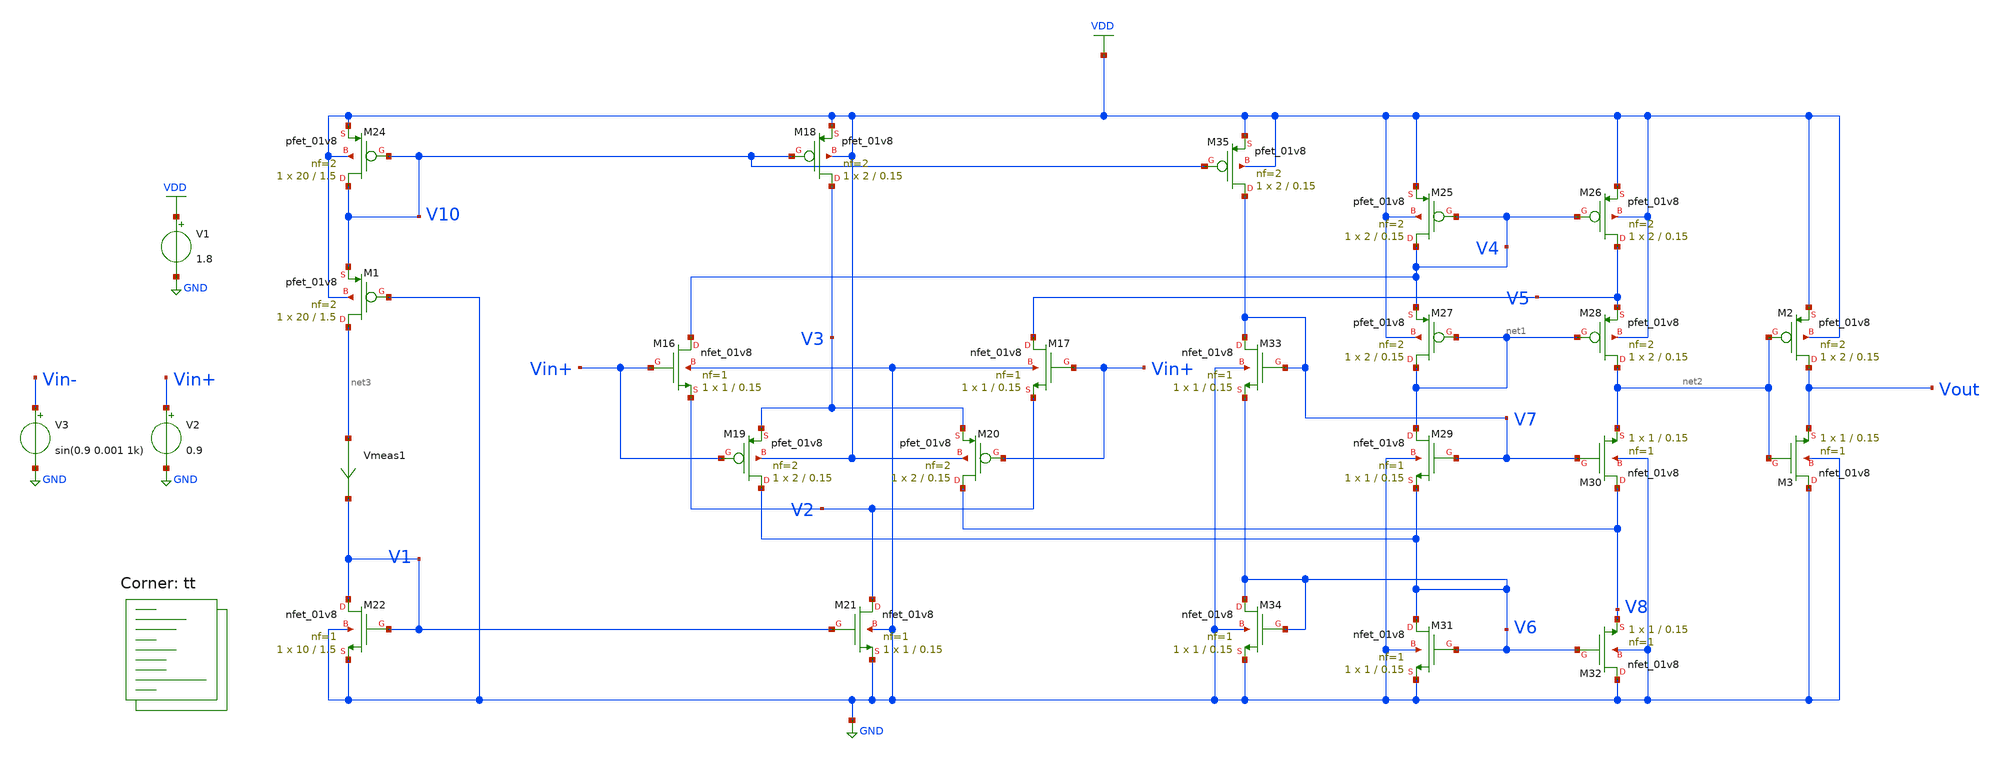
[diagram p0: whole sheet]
** sch_path: projects/pll/charge_pump/xschem_ngspice/tb_rail_to_rail_opamp2.sch
**.subckt tb_rail_to_rail_opamp2
V1 VDD GND 1.8
V3 Vin- GND sin(0.9 0.001 1k)
V2 Vin+ GND 0.9
XM16 V4 Vin+ V2 GND sky130_fd_pr__nfet_01v8 L=0.15 W=1 nf=1 ad='int((nf+1)/2) * W/nf * 0.29' as='int((nf+2)/2) * W/nf * 0.29'
+ pd='2*int((nf+1)/2) * (W/nf + 0.29)' ps='2*int((nf+2)/2) * (W/nf + 0.29)' nrd='0.29 / W' nrs='0.29 / W'
+ sa=0 sb=0 sd=0 mult=1 m=1
XM17 V5 Vin+ V2 GND sky130_fd_pr__nfet_01v8 L=0.15 W=1 nf=1 ad='int((nf+1)/2) * W/nf * 0.29' as='int((nf+2)/2) * W/nf * 0.29'
+ pd='2*int((nf+1)/2) * (W/nf + 0.29)' ps='2*int((nf+2)/2) * (W/nf + 0.29)' nrd='0.29 / W' nrs='0.29 / W'
+ sa=0 sb=0 sd=0 mult=1 m=1
XM18 V3 V10 VDD VDD sky130_fd_pr__pfet_01v8 L=0.15 W=2 nf=2 ad='int((nf+1)/2) * W/nf * 0.29' as='int((nf+2)/2) * W/nf * 0.29'
+ pd='2*int((nf+1)/2) * (W/nf + 0.29)' ps='2*int((nf+2)/2) * (W/nf + 0.29)' nrd='0.29 / W' nrs='0.29 / W'
+ sa=0 sb=0 sd=0 mult=1 m=1
XM19 V6 Vin+ V3 VDD sky130_fd_pr__pfet_01v8 L=0.15 W=2 nf=2 ad='int((nf+1)/2) * W/nf * 0.29' as='int((nf+2)/2) * W/nf * 0.29'
+ pd='2*int((nf+1)/2) * (W/nf + 0.29)' ps='2*int((nf+2)/2) * (W/nf + 0.29)' nrd='0.29 / W' nrs='0.29 / W'
+ sa=0 sb=0 sd=0 mult=1 m=1
XM20 V8 Vin+ V3 VDD sky130_fd_pr__pfet_01v8 L=0.15 W=2 nf=2 ad='int((nf+1)/2) * W/nf * 0.29' as='int((nf+2)/2) * W/nf * 0.29'
+ pd='2*int((nf+1)/2) * (W/nf + 0.29)' ps='2*int((nf+2)/2) * (W/nf + 0.29)' nrd='0.29 / W' nrs='0.29 / W'
+ sa=0 sb=0 sd=0 mult=1 m=1
XM21 V2 V1 GND GND sky130_fd_pr__nfet_01v8 L=0.15 W=1 nf=1 ad='int((nf+1)/2) * W/nf * 0.29' as='int((nf+2)/2) * W/nf * 0.29'
+ pd='2*int((nf+1)/2) * (W/nf + 0.29)' ps='2*int((nf+2)/2) * (W/nf + 0.29)' nrd='0.29 / W' nrs='0.29 / W'
+ sa=0 sb=0 sd=0 mult=1 m=1
XM22 V1 V1 GND GND sky130_fd_pr__nfet_01v8 L=1.5 W=10 nf=1 ad='int((nf+1)/2) * W/nf * 0.29' as='int((nf+2)/2) * W/nf * 0.29'
+ pd='2*int((nf+1)/2) * (W/nf + 0.29)' ps='2*int((nf+2)/2) * (W/nf + 0.29)' nrd='0.29 / W' nrs='0.29 / W'
+ sa=0 sb=0 sd=0 mult=1 m=1
XM24 V10 V10 VDD VDD sky130_fd_pr__pfet_01v8 L=1.5 W=20 nf=2 ad='int((nf+1)/2) * W/nf * 0.29' as='int((nf+2)/2) * W/nf * 0.29'
+ pd='2*int((nf+1)/2) * (W/nf + 0.29)' ps='2*int((nf+2)/2) * (W/nf + 0.29)' nrd='0.29 / W' nrs='0.29 / W'
+ sa=0 sb=0 sd=0 mult=1 m=1
XM25 V4 V4 VDD VDD sky130_fd_pr__pfet_01v8 L=0.15 W=2 nf=2 ad='int((nf+1)/2) * W/nf * 0.29' as='int((nf+2)/2) * W/nf * 0.29'
+ pd='2*int((nf+1)/2) * (W/nf + 0.29)' ps='2*int((nf+2)/2) * (W/nf + 0.29)' nrd='0.29 / W' nrs='0.29 / W'
+ sa=0 sb=0 sd=0 mult=1 m=1
XM26 V5 V4 VDD VDD sky130_fd_pr__pfet_01v8 L=0.15 W=2 nf=2 ad='int((nf+1)/2) * W/nf * 0.29' as='int((nf+2)/2) * W/nf * 0.29'
+ pd='2*int((nf+1)/2) * (W/nf + 0.29)' ps='2*int((nf+2)/2) * (W/nf + 0.29)' nrd='0.29 / W' nrs='0.29 / W'
+ sa=0 sb=0 sd=0 mult=1 m=1
XM27 net1 net1 V4 VDD sky130_fd_pr__pfet_01v8 L=0.15 W=2 nf=2 ad='int((nf+1)/2) * W/nf * 0.29' as='int((nf+2)/2) * W/nf * 0.29'
+ pd='2*int((nf+1)/2) * (W/nf + 0.29)' ps='2*int((nf+2)/2) * (W/nf + 0.29)' nrd='0.29 / W' nrs='0.29 / W'
+ sa=0 sb=0 sd=0 mult=1 m=1
XM28 net2 net1 V5 VDD sky130_fd_pr__pfet_01v8 L=0.15 W=2 nf=2 ad='int((nf+1)/2) * W/nf * 0.29' as='int((nf+2)/2) * W/nf * 0.29'
+ pd='2*int((nf+1)/2) * (W/nf + 0.29)' ps='2*int((nf+2)/2) * (W/nf + 0.29)' nrd='0.29 / W' nrs='0.29 / W'
+ sa=0 sb=0 sd=0 mult=1 m=1
XM29 net1 V7 V6 GND sky130_fd_pr__nfet_01v8 L=0.15 W=1 nf=1 ad='int((nf+1)/2) * W/nf * 0.29' as='int((nf+2)/2) * W/nf * 0.29'
+ pd='2*int((nf+1)/2) * (W/nf + 0.29)' ps='2*int((nf+2)/2) * (W/nf + 0.29)' nrd='0.29 / W' nrs='0.29 / W'
+ sa=0 sb=0 sd=0 mult=1 m=1
XM30 V8 V7 net2 GND sky130_fd_pr__nfet_01v8 L=0.15 W=1 nf=1 ad='int((nf+1)/2) * W/nf * 0.29' as='int((nf+2)/2) * W/nf * 0.29'
+ pd='2*int((nf+1)/2) * (W/nf + 0.29)' ps='2*int((nf+2)/2) * (W/nf + 0.29)' nrd='0.29 / W' nrs='0.29 / W'
+ sa=0 sb=0 sd=0 mult=1 m=1
XM31 V6 V6 GND GND sky130_fd_pr__nfet_01v8 L=0.15 W=1 nf=1 ad='int((nf+1)/2) * W/nf * 0.29' as='int((nf+2)/2) * W/nf * 0.29'
+ pd='2*int((nf+1)/2) * (W/nf + 0.29)' ps='2*int((nf+2)/2) * (W/nf + 0.29)' nrd='0.29 / W' nrs='0.29 / W'
+ sa=0 sb=0 sd=0 mult=1 m=1
XM32 GND V6 V8 GND sky130_fd_pr__nfet_01v8 L=0.15 W=1 nf=1 ad='int((nf+1)/2) * W/nf * 0.29' as='int((nf+2)/2) * W/nf * 0.29'
+ pd='2*int((nf+1)/2) * (W/nf + 0.29)' ps='2*int((nf+2)/2) * (W/nf + 0.29)' nrd='0.29 / W' nrs='0.29 / W'
+ sa=0 sb=0 sd=0 mult=1 m=1
XM33 V7 V7 V6 GND sky130_fd_pr__nfet_01v8 L=0.15 W=1 nf=1 ad='int((nf+1)/2) * W/nf * 0.29' as='int((nf+2)/2) * W/nf * 0.29'
+ pd='2*int((nf+1)/2) * (W/nf + 0.29)' ps='2*int((nf+2)/2) * (W/nf + 0.29)' nrd='0.29 / W' nrs='0.29 / W'
+ sa=0 sb=0 sd=0 mult=1 m=1
XM34 V6 V6 GND GND sky130_fd_pr__nfet_01v8 L=0.15 W=1 nf=1 ad='int((nf+1)/2) * W/nf * 0.29' as='int((nf+2)/2) * W/nf * 0.29'
+ pd='2*int((nf+1)/2) * (W/nf + 0.29)' ps='2*int((nf+2)/2) * (W/nf + 0.29)' nrd='0.29 / W' nrs='0.29 / W'
+ sa=0 sb=0 sd=0 mult=1 m=1
XM35 V7 V10 VDD VDD sky130_fd_pr__pfet_01v8 L=0.15 W=2 nf=2 ad='int((nf+1)/2) * W/nf * 0.29' as='int((nf+2)/2) * W/nf * 0.29'
+ pd='2*int((nf+1)/2) * (W/nf + 0.29)' ps='2*int((nf+2)/2) * (W/nf + 0.29)' nrd='0.29 / W' nrs='0.29 / W'
+ sa=0 sb=0 sd=0 mult=1 m=1
XM1 net3 GND V10 VDD sky130_fd_pr__pfet_01v8 L=1.5 W=20 nf=2 ad='int((nf+1)/2) * W/nf * 0.29' as='int((nf+2)/2) * W/nf * 0.29'
+ pd='2*int((nf+1)/2) * (W/nf + 0.29)' ps='2*int((nf+2)/2) * (W/nf + 0.29)' nrd='0.29 / W' nrs='0.29 / W'
+ sa=0 sb=0 sd=0 mult=1 m=1
Vmeas1 net3 V1 0
.save i(vmeas1)
XM2 Vout net2 VDD VDD sky130_fd_pr__pfet_01v8 L=0.15 W=2 nf=2 ad='int((nf+1)/2) * W/nf * 0.29' as='int((nf+2)/2) * W/nf * 0.29'
+ pd='2*int((nf+1)/2) * (W/nf + 0.29)' ps='2*int((nf+2)/2) * (W/nf + 0.29)' nrd='0.29 / W' nrs='0.29 / W'
+ sa=0 sb=0 sd=0 mult=1 m=1
XM3 GND net2 Vout GND sky130_fd_pr__nfet_01v8 L=0.15 W=1 nf=1 ad='int((nf+1)/2) * W/nf * 0.29' as='int((nf+2)/2) * W/nf * 0.29'
+ pd='2*int((nf+1)/2) * (W/nf + 0.29)' ps='2*int((nf+2)/2) * (W/nf + 0.29)' nrd='0.29 / W' nrs='0.29 / W'
+ sa=0 sb=0 sd=0 mult=1 m=1
**** begin user architecture code



.option wnflag=1
* .option savecurrents

.control

    save all
  * tran 1u 8m
  * ac dec 20 1 1T
    dc V2 0 1.8 0.01
  write tb_rail_to_rail_opamp2.raw
    set appendwrite

.endc



.lib $::SKYWATER_MODELS/sky130.lib.spice tt
**** end user architecture code
**.ends
.GLOBAL GND
.GLOBAL VDD
.end
